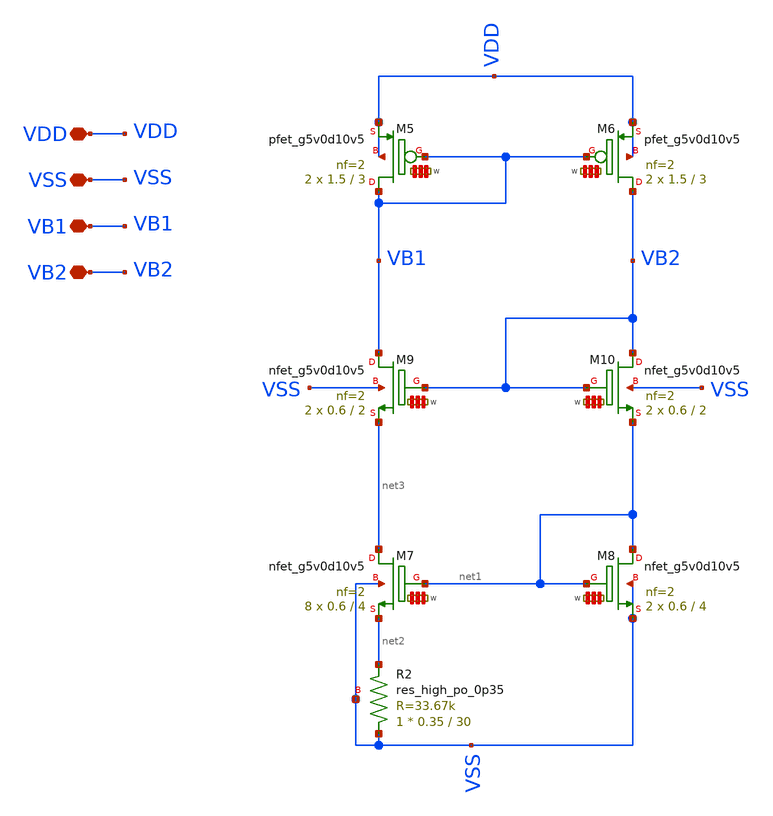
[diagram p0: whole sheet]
** sch_path: Learning/single_ended_amplifiers/Design_transcondutance_cell_sky130_5V/layout_example/pmos_current_mirror_old/transimpedance_example.sch
**.subckt transimpedance_example VDD VSS VB1 VB2
*.iopin VDD
*.iopin VSS
*.iopin VB1
*.iopin VB2
XM5 VB1 VB1 VDD VDD sky130_fd_pr__pfet_g5v0d10v5 L=3 W='1.5 * 2 ' nf=2 ad='int((2 + 1)/2) * 1.5 * 0.29'
+ as='int((2 + 2)/2) * 1.5 * 0.29' pd='2*int((2 + 1)/2) * (1.5 + 0.29)' ps='2*int((2 + 2)/2) * (1.5 + 0.29)'
+ nrd='0.29 / 1.5 / 2 ' nrs='0.29 / 1.5 / 2 ' sa=0 sb=0 sd=0 mult=2 m=2
XM6 VB2 VB1 VDD VDD sky130_fd_pr__pfet_g5v0d10v5 L=3 W='1.5 * 2 ' nf=2 ad='int((2 + 1)/2) * 1.5 * 0.29'
+ as='int((2 + 2)/2) * 1.5 * 0.29' pd='2*int((2 + 1)/2) * (1.5 + 0.29)' ps='2*int((2 + 2)/2) * (1.5 + 0.29)'
+ nrd='0.29 / 1.5 / 2 ' nrs='0.29 / 1.5 / 2 ' sa=0 sb=0 sd=0 mult=2 m=2
XM7 net3 net1 net2 VSS sky130_fd_pr__nfet_g5v0d10v5 L=4 W='0.6 * 2 ' nf=2 ad='int((nf+1)/2) * W / nf * 0.29'
+ as='int((nf+2)/2) * W / nf * 0.29' pd='2*int((nf+1)/2) * (W / nf + 0.29)' ps='2*int((nf+2)/2) * (W / nf + 0.29)'
+ nrd='0.29 / W ' nrs='0.29 / W ' sa=0 sb=0 sd=0 mult=8 m=8
XM8 net1 net1 VSS VSS sky130_fd_pr__nfet_g5v0d10v5 L=4 W='0.6 * 2 ' nf=2 ad='int((nf+1)/2) * W / nf * 0.29'
+ as='int((nf+2)/2) * W / nf * 0.29' pd='2*int((nf+1)/2) * (W / nf + 0.29)' ps='2*int((nf+2)/2) * (W / nf + 0.29)'
+ nrd='0.29 / W ' nrs='0.29 / W ' sa=0 sb=0 sd=0 mult=2 m=2
XM9 VB1 VB2 net3 VSS sky130_fd_pr__nfet_g5v0d10v5 L=2 W='0.6 * 2 ' nf=2 ad='int((nf+1)/2) * W / nf * 0.29'
+ as='int((nf+2)/2) * W / nf * 0.29' pd='2*int((nf+1)/2) * (W / nf + 0.29)' ps='2*int((nf+2)/2) * (W / nf + 0.29)'
+ nrd='0.29 / W ' nrs='0.29 / W ' sa=0 sb=0 sd=0 mult=2 m=2
XM10 VB2 VB2 net1 VSS sky130_fd_pr__nfet_g5v0d10v5 L=2 W='0.6 * 2 ' nf=2 ad='int((nf+1)/2) * W / nf * 0.29'
+ as='int((nf+2)/2) * W / nf * 0.29' pd='2*int((nf+1)/2) * (W / nf + 0.29)' ps='2*int((nf+2)/2) * (W / nf + 0.29)'
+ nrd='0.29 / W ' nrs='0.29 / W ' sa=0 sb=0 sd=0 mult=2 m=2
XR2 VSS net2 VSS sky130_fd_pr__res_high_po_0p35 L=30 mult=1 m=1
**.ends
.end
